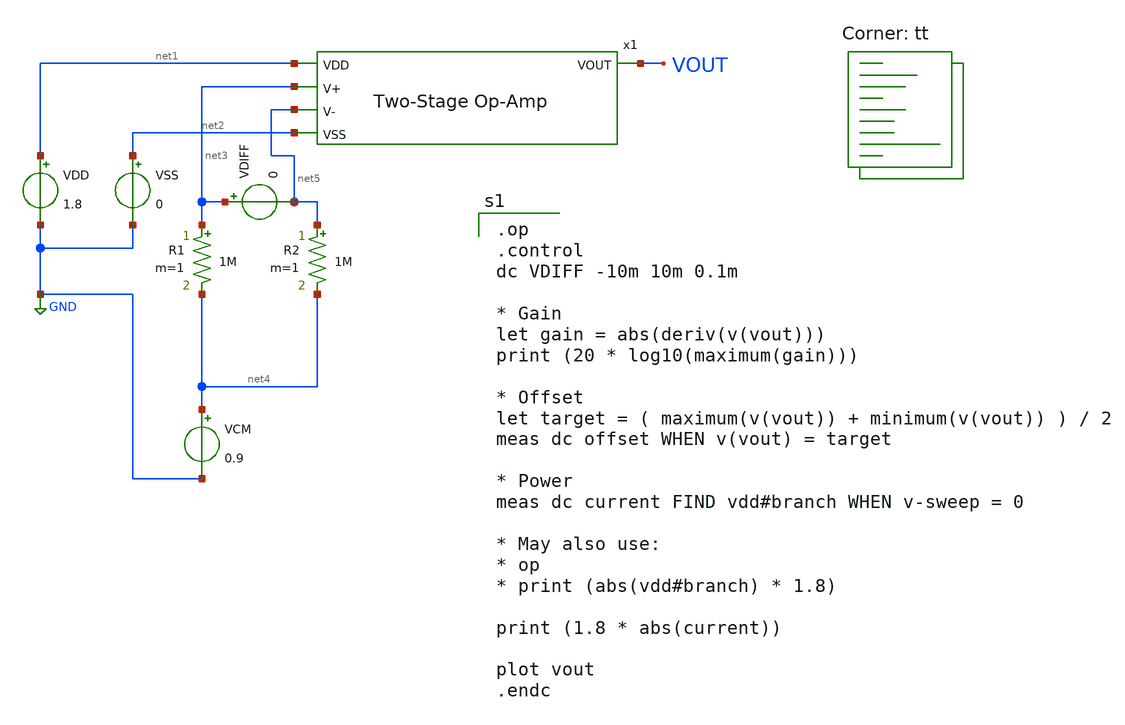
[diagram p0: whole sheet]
** sch_path: analog/schematics/tb_dc_analysis.sch
**.subckt tb_dc_analysis
VDD net1 GND 1.8
VSS net2 GND 0
VCM net4 GND 0.9
VDIFF net3 net5 0
R1 net3 net4 1M m=1
R2 net5 net4 1M m=1
x1 net1 net3 net5 VOUT net2 bootcamp_opamp
**** begin user architecture code

.op
.control
dc VDIFF -10m 10m 0.1m

* Gain
let gain = abs(deriv(v(vout)))
print (20 * log10(maximum(gain)))

* Offset
let target = ( maximum(v(vout)) + minimum(v(vout)) ) / 2
meas dc offset WHEN v(vout) = target

* Power
meas dc current FIND vdd#branch WHEN v-sweep = 0

* May also use:
* op
* print (abs(vdd#branch) * 1.8)

print (1.8 * abs(current))

plot vout
.endc

.lib $::SKYWATER_MODELS/sky130.lib.spice tt
**** end user architecture code
**.ends

* expanding   symbol:  bootcamp_opamp.sym # of pins=5
** sym_path: analog/schematics/bootcamp_opamp.sym
** sch_path: analog/schematics/bootcamp_opamp.sch
.subckt bootcamp_opamp VDD V+ V- VOUT VSS
*.ipin V+
*.ipin V-
*.opin VOUT
*.ipin VDD
*.ipin VSS
XM1 net1 V+ net3 VSS sky130_fd_pr__nfet_01v8 L=1 W=4 nf=1 ad='int((nf+1)/2) * W/nf * 0.29' as='int((nf+2)/2) * W/nf * 0.29'
+ pd='2*int((nf+1)/2) * (W/nf + 0.29)' ps='2*int((nf+2)/2) * (W/nf + 0.29)' nrd='0.29 / W' nrs='0.29 / W'
+ sa=0 sb=0 sd=0 mult=1 m=1
XM2 net2 V- net3 VSS sky130_fd_pr__nfet_01v8 L=1 W=4 nf=1 ad='int((nf+1)/2) * W/nf * 0.29' as='int((nf+2)/2) * W/nf * 0.29'
+ pd='2*int((nf+1)/2) * (W/nf + 0.29)' ps='2*int((nf+2)/2) * (W/nf + 0.29)' nrd='0.29 / W' nrs='0.29 / W'
+ sa=0 sb=0 sd=0 mult=1 m=1
XM3 net1 net1 VDD VDD sky130_fd_pr__pfet_01v8 L=1 W=4 nf=1 ad='int((nf+1)/2) * W/nf * 0.29' as='int((nf+2)/2) * W/nf * 0.29'
+ pd='2*int((nf+1)/2) * (W/nf + 0.29)' ps='2*int((nf+2)/2) * (W/nf + 0.29)' nrd='0.29 / W' nrs='0.29 / W'
+ sa=0 sb=0 sd=0 mult=1 m=1
XM4 net2 net1 VDD VDD sky130_fd_pr__pfet_01v8 L=1 W=4 nf=1 ad='int((nf+1)/2) * W/nf * 0.29' as='int((nf+2)/2) * W/nf * 0.29'
+ pd='2*int((nf+1)/2) * (W/nf + 0.29)' ps='2*int((nf+2)/2) * (W/nf + 0.29)' nrd='0.29 / W' nrs='0.29 / W'
+ sa=0 sb=0 sd=0 mult=1 m=1
XM5 net3 net4 VSS VSS sky130_fd_pr__nfet_01v8 L=2 W=4 nf=1 ad='int((nf+1)/2) * W/nf * 0.29' as='int((nf+2)/2) * W/nf * 0.29'
+ pd='2*int((nf+1)/2) * (W/nf + 0.29)' ps='2*int((nf+2)/2) * (W/nf + 0.29)' nrd='0.29 / W' nrs='0.29 / W'
+ sa=0 sb=0 sd=0 mult=1 m=1
XM6 net4 net4 VSS VSS sky130_fd_pr__nfet_01v8 L=2 W=4 nf=1 ad='int((nf+1)/2) * W/nf * 0.29' as='int((nf+2)/2) * W/nf * 0.29'
+ pd='2*int((nf+1)/2) * (W/nf + 0.29)' ps='2*int((nf+2)/2) * (W/nf + 0.29)' nrd='0.29 / W' nrs='0.29 / W'
+ sa=0 sb=0 sd=0 mult=1 m=1
XM8 VOUT net4 VSS VSS sky130_fd_pr__nfet_01v8 L=0.5 W=2 nf=1 ad='int((nf+1)/2) * W/nf * 0.29' as='int((nf+2)/2) * W/nf * 0.29'
+ pd='2*int((nf+1)/2) * (W/nf + 0.29)' ps='2*int((nf+2)/2) * (W/nf + 0.29)' nrd='0.29 / W' nrs='0.29 / W'
+ sa=0 sb=0 sd=0 mult=1 m=1
XC1 net2 VOUT sky130_fd_pr__cap_mim_m3_1 W=22 L=22 MF=1 m=1
R1 VDD net4 12k m=1
XM7 VOUT net2 VDD VDD sky130_fd_pr__pfet_01v8 L=0.5 W=8 nf=1 ad='int((nf+1)/2) * W/nf * 0.29' as='int((nf+2)/2) * W/nf * 0.29'
+ pd='2*int((nf+1)/2) * (W/nf + 0.29)' ps='2*int((nf+2)/2) * (W/nf + 0.29)' nrd='0.29 / W' nrs='0.29 / W'
+ sa=0 sb=0 sd=0 mult=1 m=1
.ends

.GLOBAL GND
.end
